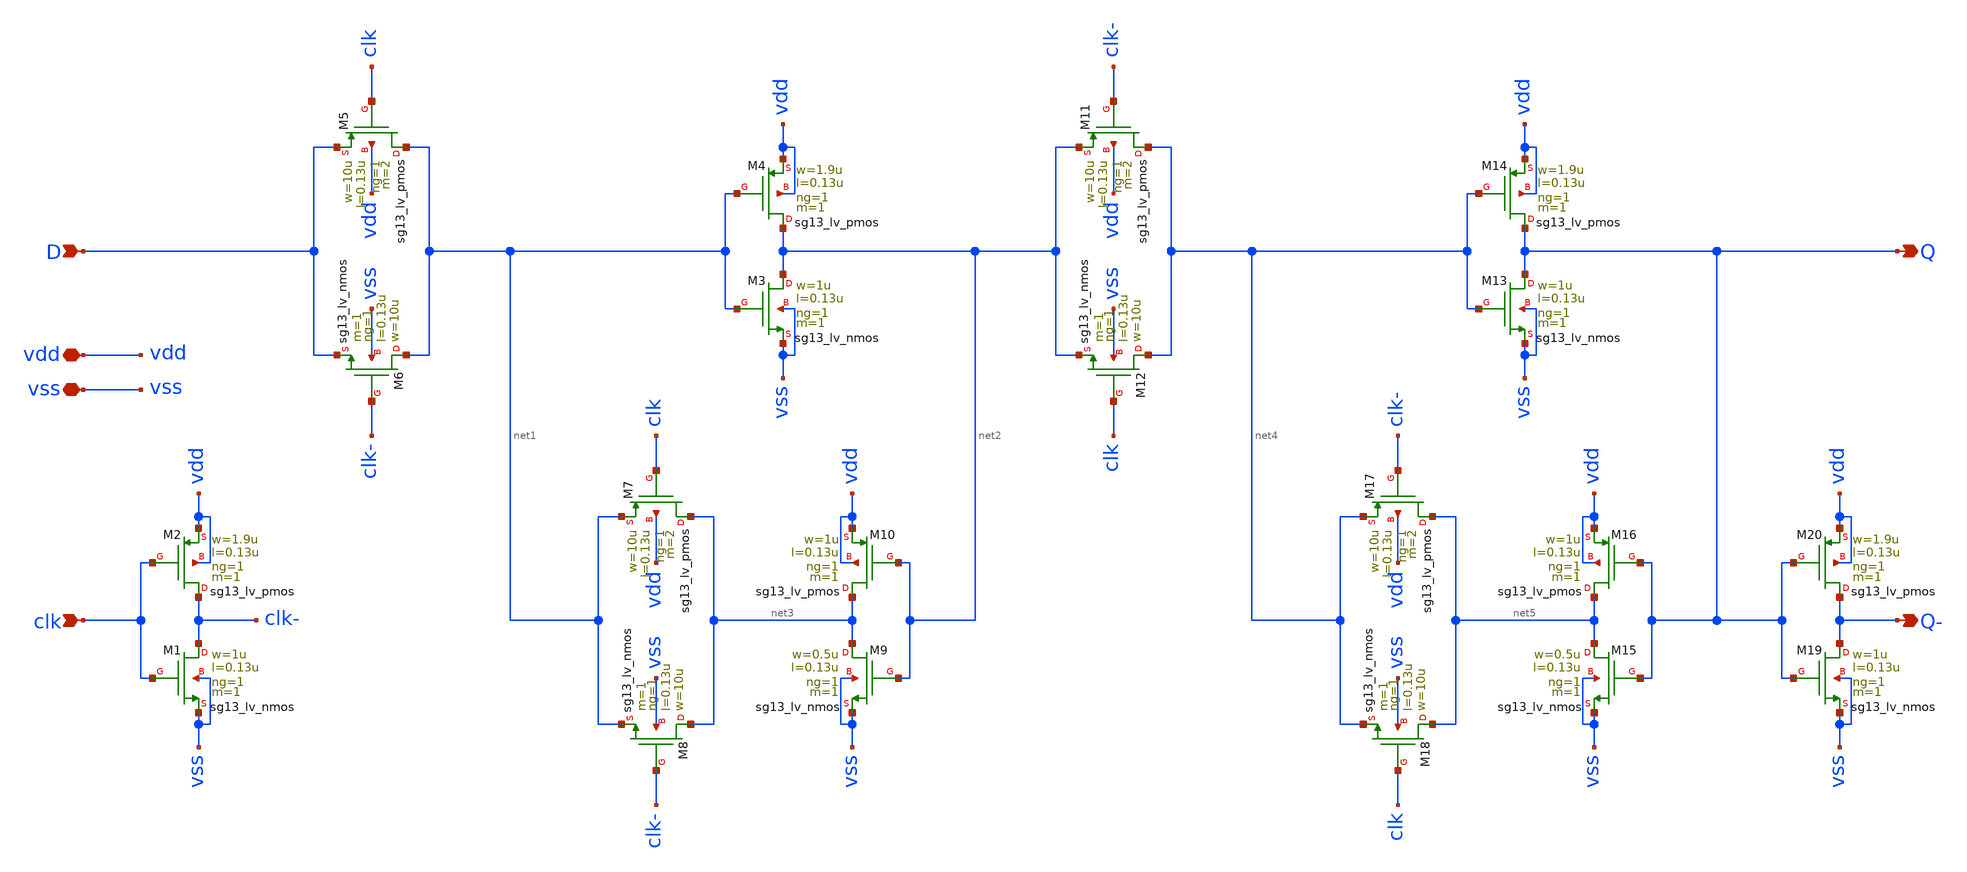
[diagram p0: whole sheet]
** sch_path: SSDOR_1.2V_v2/components/cgenerator/dff.sch
**.subckt dff clk vdd Q vss D Q-
*.ipin clk
*.iopin vdd
*.opin Q
*.iopin vss
*.ipin D
*.opin Q-
XM1 clk- clk vss vss sg13_lv_nmos w=1u l=0.13u ng=1 m=1 mm_ok=1
XM2 clk- clk vdd vdd sg13_lv_pmos w=1.9u l=0.13u ng=1 m=1 mm_ok=1
XM3 net2 net1 vss vss sg13_lv_nmos w=1u l=0.13u ng=1 m=1 mm_ok=1
XM4 net2 net1 vdd vdd sg13_lv_pmos w=1.9u l=0.13u ng=1 m=1 mm_ok=1
XM5 net1 clk D vdd sg13_lv_pmos w=10u l=0.13u ng=1 m=2 mm_ok=1
XM6 net1 clk- D vss sg13_lv_nmos w=10u l=0.13u ng=1 m=1 mm_ok=1
XM9 net3 net2 vss vss sg13_lv_nmos w=0.5u l=0.13u ng=1 m=1 mm_ok=1
XM10 net3 net2 vdd vdd sg13_lv_pmos w=1u l=0.13u ng=1 m=1 mm_ok=1
XM7 net3 clk net1 vdd sg13_lv_pmos w=10u l=0.13u ng=1 m=2 mm_ok=1
XM8 net3 clk- net1 vss sg13_lv_nmos w=10u l=0.13u ng=1 m=1 mm_ok=1
XM11 net4 clk- net2 vdd sg13_lv_pmos w=10u l=0.13u ng=1 m=2 mm_ok=1
XM12 net4 clk net2 vss sg13_lv_nmos w=10u l=0.13u ng=1 m=1 mm_ok=1
XM13 Q net4 vss vss sg13_lv_nmos w=1u l=0.13u ng=1 m=1 mm_ok=1
XM14 Q net4 vdd vdd sg13_lv_pmos w=1.9u l=0.13u ng=1 m=1 mm_ok=1
XM15 net5 Q vss vss sg13_lv_nmos w=0.5u l=0.13u ng=1 m=1 mm_ok=1
XM16 net5 Q vdd vdd sg13_lv_pmos w=1u l=0.13u ng=1 m=1 mm_ok=1
XM17 net5 clk- net4 vdd sg13_lv_pmos w=10u l=0.13u ng=1 m=2 mm_ok=1
XM18 net5 clk net4 vss sg13_lv_nmos w=10u l=0.13u ng=1 m=1 mm_ok=1
XM19 Q- Q vss vss sg13_lv_nmos w=1u l=0.13u ng=1 m=1 mm_ok=1
XM20 Q- Q vdd vdd sg13_lv_pmos w=1.9u l=0.13u ng=1 m=1 mm_ok=1
**.ends
.end
